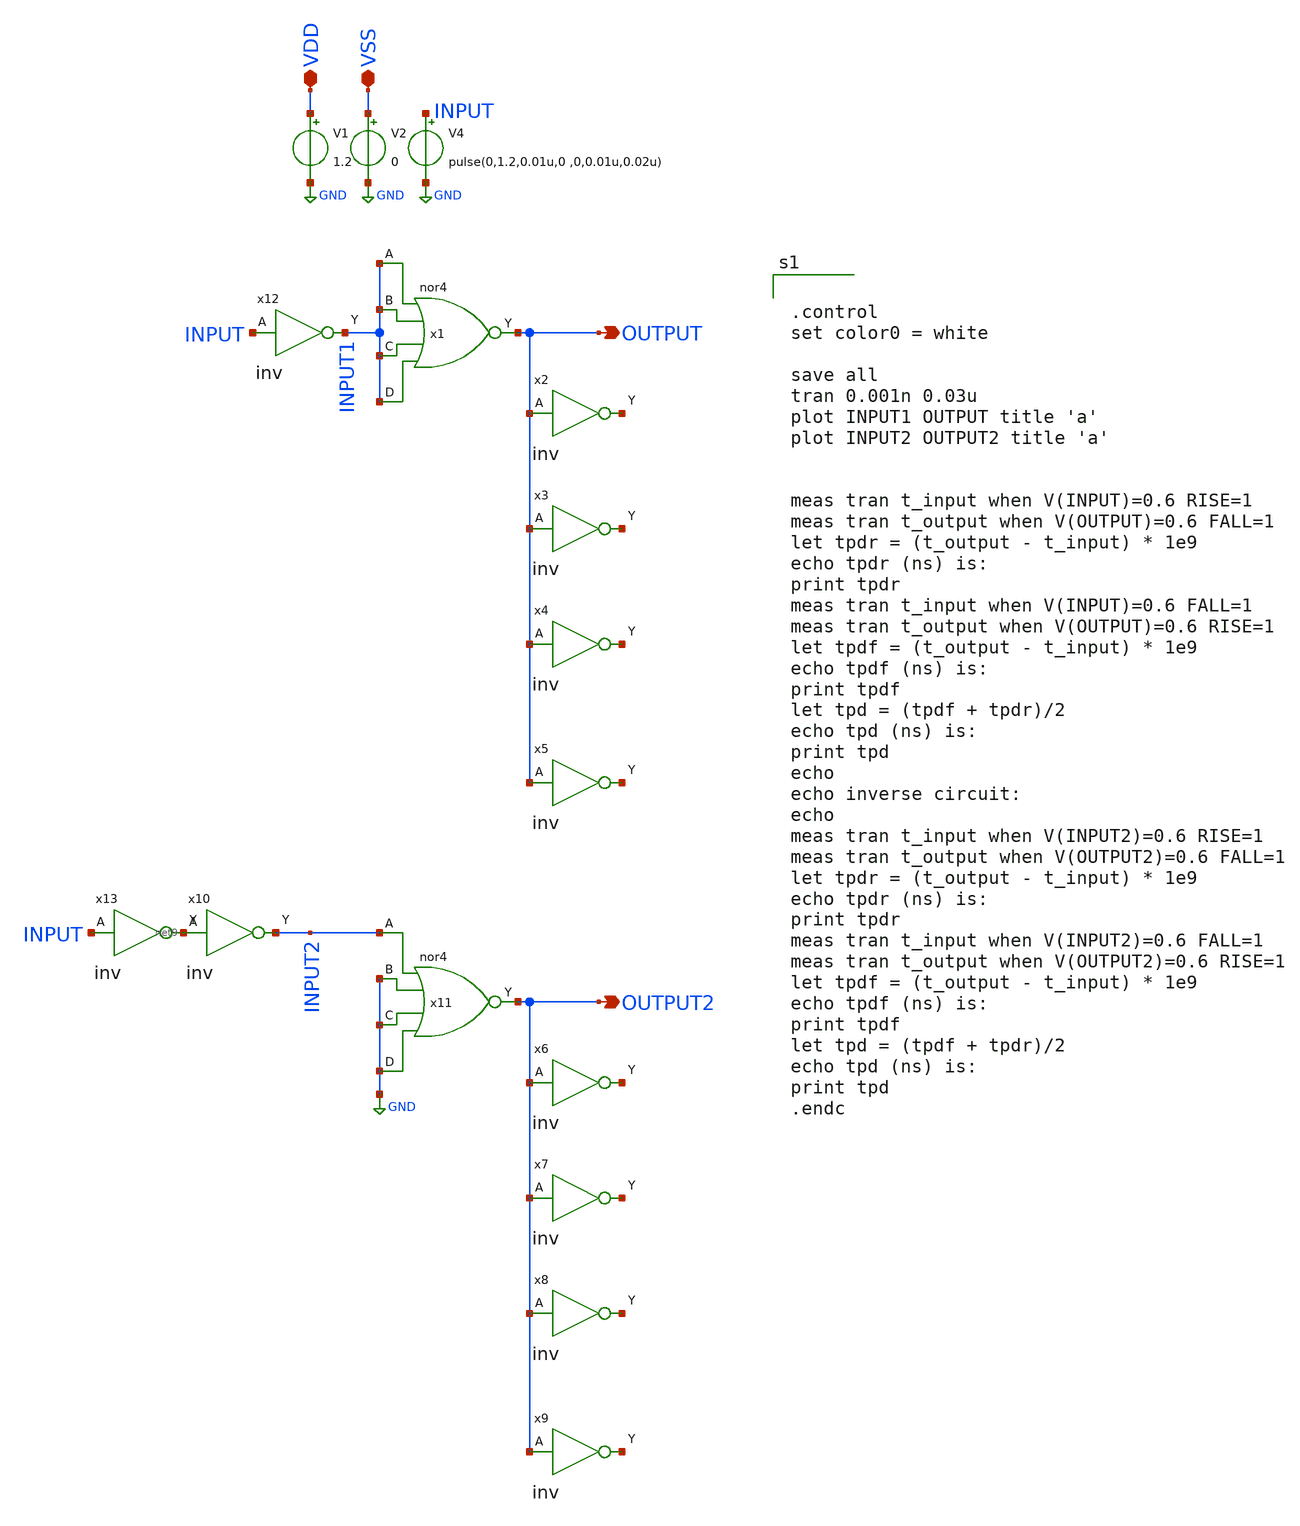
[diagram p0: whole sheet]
** sch_path: design/xschem/NOR/nor4_TB.sch
**.subckt nor4_TB OUTPUT VDD VSS OUTPUT2
*.opin OUTPUT
*.iopin VDD
*.iopin VSS
*.opin OUTPUT2
V1 VDD GND 1.2
V2 VSS GND 0
V4 INPUT GND pulse(0,1.2,0.01u,0 ,0,0.01u,0.02u)
x2 OUTPUT VSS VDD net1 inv
x3 OUTPUT VSS VDD net2 inv
x4 OUTPUT VSS VDD net3 inv
x5 OUTPUT VSS VDD net4 inv
x6 OUTPUT2 VSS VDD net5 inv
x7 OUTPUT2 VSS VDD net6 inv
x8 OUTPUT2 VSS VDD net7 inv
x9 OUTPUT2 VSS VDD net8 inv
x10 net9 VSS VDD INPUT2 inv
x12 INPUT VSS VDD INPUT1 inv
x13 INPUT VSS VDD net9 inv
x1 INPUT1 INPUT1 INPUT1 INPUT1 VSS VDD OUTPUT nor4
x11 INPUT2 GND GND GND VSS VDD OUTPUT2 nor4
**** begin user architecture code

** opencircuitdesign pdks install
.lib $::SKYWATER_MODELS/sky130.lib.spice tt_mm




.control
set color0 = white

save all
tran 0.001n 0.03u
plot INPUT1 OUTPUT title 'a'
plot INPUT2 OUTPUT2 title 'a'


meas tran t_input when V(INPUT)=0.6 RISE=1
meas tran t_output when V(OUTPUT)=0.6 FALL=1
let tpdr = (t_output - t_input) * 1e9
echo tpdr (ns) is:
print tpdr
meas tran t_input when V(INPUT)=0.6 FALL=1
meas tran t_output when V(OUTPUT)=0.6 RISE=1
let tpdf = (t_output - t_input) * 1e9
echo tpdf (ns) is:
print tpdf
let tpd = (tpdf + tpdr)/2
echo tpd (ns) is:
print tpd
echo
echo inverse circuit:
echo
meas tran t_input when V(INPUT2)=0.6 RISE=1
meas tran t_output when V(OUTPUT2)=0.6 FALL=1
let tpdr = (t_output - t_input) * 1e9
echo tpdr (ns) is:
print tpdr
meas tran t_input when V(INPUT2)=0.6 FALL=1
meas tran t_output when V(OUTPUT2)=0.6 RISE=1
let tpdf = (t_output - t_input) * 1e9
echo tpdf (ns) is:
print tpdf
let tpd = (tpdf + tpdr)/2
echo tpd (ns) is:
print tpd
.endc


**** end user architecture code
**.ends

* expanding   symbol:  INV/inv.sym # of pins=2
** sym_path: design/xschem/INV/inv.sym
** sch_path: design/xschem/INV/inv.sch
.subckt inv A VSS VDD Y
*.ipin A
*.opin Y
XM2 Y A VSS GND sky130_fd_pr__nfet_01v8 L=0.15 W=1 nf=1 ad='int((nf+1)/2) * W/nf * 0.29' as='int((nf+2)/2) * W/nf * 0.29'
+ pd='2*int((nf+1)/2) * (W/nf + 0.29)' ps='2*int((nf+2)/2) * (W/nf + 0.29)' nrd='0.29 / W' nrs='0.29 / W'
+ sa=0 sb=0 sd=0 mult=1 m=1
XM1 Y A VDD VDD sky130_fd_pr__pfet_01v8 L=0.15 W=3.21 nf=1 ad='int((nf+1)/2) * W/nf * 0.29' as='int((nf+2)/2) * W/nf * 0.29'
+ pd='2*int((nf+1)/2) * (W/nf + 0.29)' ps='2*int((nf+2)/2) * (W/nf + 0.29)' nrd='0.29 / W' nrs='0.29 / W'
+ sa=0 sb=0 sd=0 mult=1 m=1
.ends


* expanding   symbol:  NOR/nor4.sym # of pins=5
** sym_path: design/xschem/NOR/nor4.sym
** sch_path: design/xschem/NOR/nor4.sch
.subckt nor4 A B C D VSS VDD Y
*.ipin A
*.opin Y
*.ipin B
*.ipin C
*.ipin D
XM1 Y A net1 net1 sky130_fd_pr__pfet_01v8 L=0.15 W=12.8 nf=1 ad='int((nf+1)/2) * W/nf * 0.29' as='int((nf+2)/2) * W/nf * 0.29'
+ pd='2*int((nf+1)/2) * (W/nf + 0.29)' ps='2*int((nf+2)/2) * (W/nf + 0.29)' nrd='0.29 / W' nrs='0.29 / W'
+ sa=0 sb=0 sd=0 mult=1 m=1
XM2 Y A VSS VSS sky130_fd_pr__nfet_01v8 L=0.15 W=1 nf=1 ad='int((nf+1)/2) * W/nf * 0.29' as='int((nf+2)/2) * W/nf * 0.29'
+ pd='2*int((nf+1)/2) * (W/nf + 0.29)' ps='2*int((nf+2)/2) * (W/nf + 0.29)' nrd='0.29 / W' nrs='0.29 / W'
+ sa=0 sb=0 sd=0 mult=1 m=1
XM3 Y B VSS VSS sky130_fd_pr__nfet_01v8 L=0.15 W=1 nf=1 ad='int((nf+1)/2) * W/nf * 0.29' as='int((nf+2)/2) * W/nf * 0.29'
+ pd='2*int((nf+1)/2) * (W/nf + 0.29)' ps='2*int((nf+2)/2) * (W/nf + 0.29)' nrd='0.29 / W' nrs='0.29 / W'
+ sa=0 sb=0 sd=0 mult=1 m=1
XM4 net1 B net3 net3 sky130_fd_pr__pfet_01v8 L=0.15 W=12.8 nf=1 ad='int((nf+1)/2) * W/nf * 0.29' as='int((nf+2)/2) * W/nf * 0.29'
+ pd='2*int((nf+1)/2) * (W/nf + 0.29)' ps='2*int((nf+2)/2) * (W/nf + 0.29)' nrd='0.29 / W' nrs='0.29 / W'
+ sa=0 sb=0 sd=0 mult=1 m=1
XM5 net3 C net2 net2 sky130_fd_pr__pfet_01v8 L=0.15 W=12.8 nf=1 ad='int((nf+1)/2) * W/nf * 0.29' as='int((nf+2)/2) * W/nf * 0.29'
+ pd='2*int((nf+1)/2) * (W/nf + 0.29)' ps='2*int((nf+2)/2) * (W/nf + 0.29)' nrd='0.29 / W' nrs='0.29 / W'
+ sa=0 sb=0 sd=0 mult=1 m=1
XM6 Y C VSS VSS sky130_fd_pr__nfet_01v8 L=0.15 W=1 nf=1 ad='int((nf+1)/2) * W/nf * 0.29' as='int((nf+2)/2) * W/nf * 0.29'
+ pd='2*int((nf+1)/2) * (W/nf + 0.29)' ps='2*int((nf+2)/2) * (W/nf + 0.29)' nrd='0.29 / W' nrs='0.29 / W'
+ sa=0 sb=0 sd=0 mult=1 m=1
XM7 Y D VSS VSS sky130_fd_pr__nfet_01v8 L=0.15 W=1 nf=1 ad='int((nf+1)/2) * W/nf * 0.29' as='int((nf+2)/2) * W/nf * 0.29'
+ pd='2*int((nf+1)/2) * (W/nf + 0.29)' ps='2*int((nf+2)/2) * (W/nf + 0.29)' nrd='0.29 / W' nrs='0.29 / W'
+ sa=0 sb=0 sd=0 mult=1 m=1
XM8 net2 D VDD VDD sky130_fd_pr__pfet_01v8 L=0.15 W=12.8 nf=1 ad='int((nf+1)/2) * W/nf * 0.29' as='int((nf+2)/2) * W/nf * 0.29'
+ pd='2*int((nf+1)/2) * (W/nf + 0.29)' ps='2*int((nf+2)/2) * (W/nf + 0.29)' nrd='0.29 / W' nrs='0.29 / W'
+ sa=0 sb=0 sd=0 mult=1 m=1
.ends

.GLOBAL GND
.end
